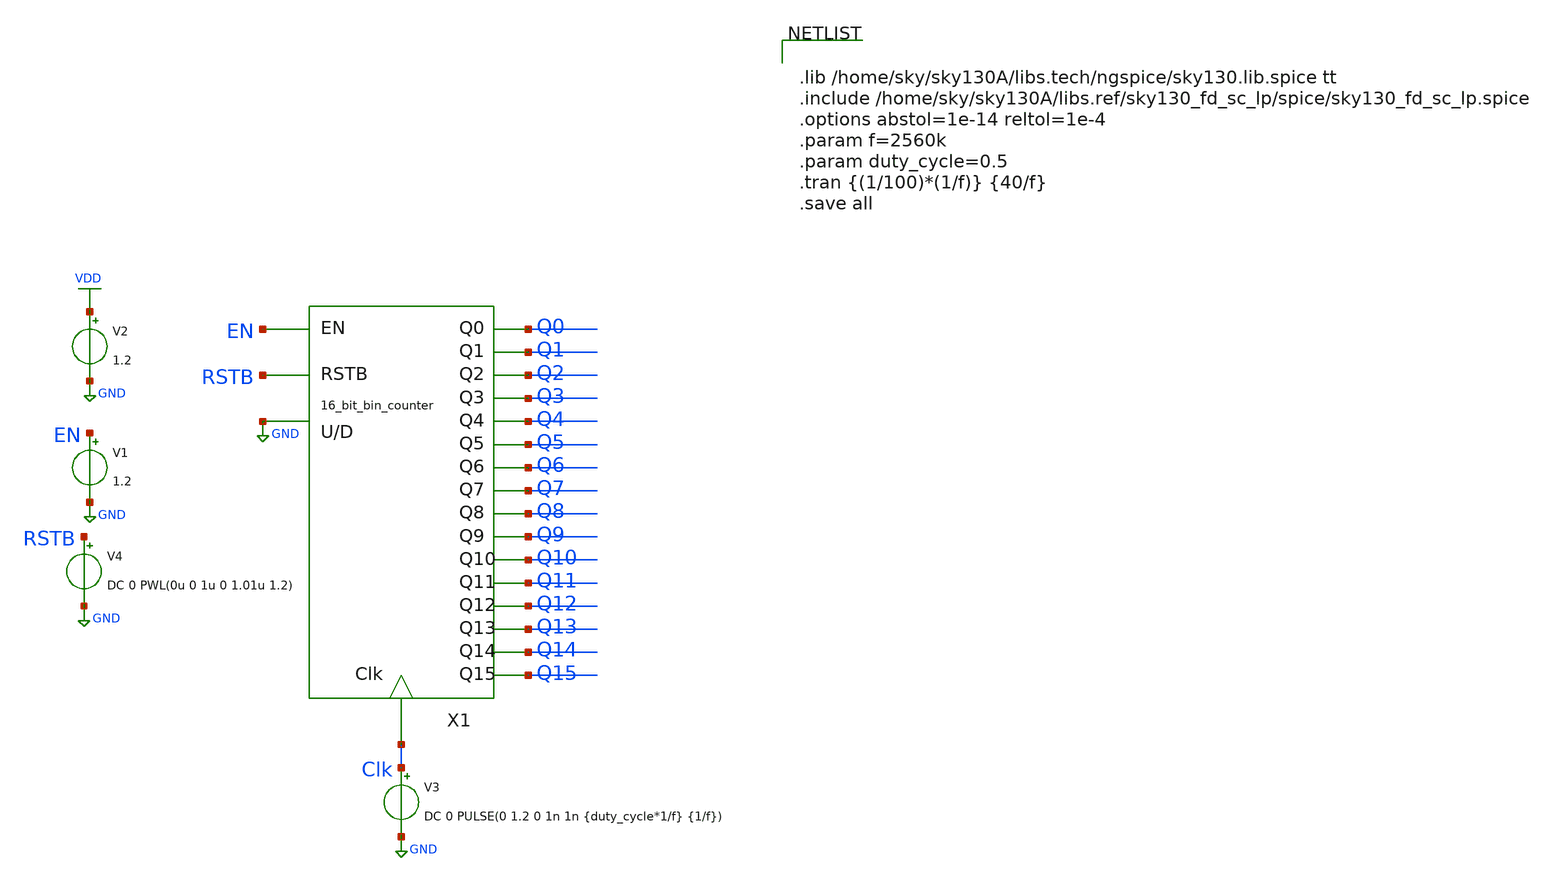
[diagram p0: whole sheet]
** sch_path: xschem/binary counter/bin_counter_tb.sch
**.subckt bin_counter_tb
V3 Clk GND DC 0 PULSE(0 1.2 0 1n 1n {duty_cycle*1/f} {1/f})
V1 EN GND 1.2
V2 VDD GND 1.2
X1 EN Q1 Q6 Clk Q0 Q2 Q3 Q4 Q5 Q7 Q8 Q9 Q10 Q11 Q12 Q13 Q14 Q15 RSTB GND bin_counter
V4 RSTB GND DC 0 PWL(0u 0 1u 0 1.01u 1.2)
**** begin user architecture code


.lib /home/sky/sky130A/libs.tech/ngspice/sky130.lib.spice tt
.include /home/sky/sky130A/libs.ref/sky130_fd_sc_lp/spice/sky130_fd_sc_lp.spice
.options abstol=1e-14 reltol=1e-4
.param f=2560k
.param duty_cycle=0.5
.tran {(1/100)*(1/f)} {40/f}
.save all


**** end user architecture code
**.ends

* expanding   symbol:  binary counter/bin_counter.sym # of pins=20
** sym_path: xschem/binary counter/bin_counter.sym
** sch_path: xschem/binary counter/bin_counter.sch
.subckt bin_counter EN Q1 Q6 Clk Q0 Q2 Q3 Q4 Q5 Q7 Q8 Q9 Q10 Q11 Q12 Q13 Q14 Q15 RSTB U/D
*.ipin Clk
*.ipin EN
*.opin Q0
*.ipin RSTB
*.ipin U/D
*.opin Q1
*.opin Q2
*.opin Q3
*.opin Q4
*.opin Q5
*.opin Q6
*.opin Q7
*.opin Q8
*.opin Q9
*.opin Q10
*.opin Q11
*.opin Q12
*.opin Q13
*.opin Q14
*.opin Q15
x16 U/D Q0 GND GND VDD VDD net1 sky130_fd_sc_lp__and2_1
X17 EN Q0 Clk RSTB net4 asyn_rst_t_ff
x17 net1 net2 GND GND VDD VDD net8 sky130_fd_sc_lp__or2_0
x18 U/D GND GND VDD VDD net3 sky130_fd_sc_lp__inv_1
x19 net4 net3 GND GND VDD VDD net2 sky130_fd_sc_lp__and2_1
x20 net1 Q1 GND GND VDD VDD net5 sky130_fd_sc_lp__and2_1
X18 T1 Q1 Clk RSTB net7 asyn_rst_t_ff
x21 net5 net6 GND GND VDD VDD net48 sky130_fd_sc_lp__or2_0
x23 net7 net2 GND GND VDD VDD net6 sky130_fd_sc_lp__and2_1
x28 net5 Q2 GND GND VDD VDD net9 sky130_fd_sc_lp__and2_1
X20 net62 Q2 Clk RSTB net11 asyn_rst_t_ff
x29 net9 net10 GND GND VDD VDD net50 sky130_fd_sc_lp__or2_0
x31 net11 net6 GND GND VDD VDD net10 sky130_fd_sc_lp__and2_1
x32 net9 Q3 GND GND VDD VDD net12 sky130_fd_sc_lp__and2_1
X21 net63 Q3 Clk RSTB net14 asyn_rst_t_ff
x33 net12 net13 GND GND VDD VDD net51 sky130_fd_sc_lp__or2_0
x35 net14 net10 GND GND VDD VDD net13 sky130_fd_sc_lp__and2_1
x36 net12 Q4 GND GND VDD VDD net15 sky130_fd_sc_lp__and2_1
X22 net64 Q4 Clk RSTB net17 asyn_rst_t_ff
x37 net15 net16 GND GND VDD VDD net49 sky130_fd_sc_lp__or2_0
x39 net17 net13 GND GND VDD VDD net16 sky130_fd_sc_lp__and2_1
x40 net15 Q5 GND GND VDD VDD net18 sky130_fd_sc_lp__and2_1
X23 net65 Q5 Clk RSTB net20 asyn_rst_t_ff
x41 net18 net19 GND GND VDD VDD net52 sky130_fd_sc_lp__or2_0
x43 net20 net16 GND GND VDD VDD net19 sky130_fd_sc_lp__and2_1
x44 net18 Q6 GND GND VDD VDD net21 sky130_fd_sc_lp__and2_1
X24 net66 Q6 Clk RSTB net23 asyn_rst_t_ff
x45 net21 net22 GND GND VDD VDD net53 sky130_fd_sc_lp__or2_0
x47 net23 net19 GND GND VDD VDD net22 sky130_fd_sc_lp__and2_1
x48 net21 Q7 GND GND VDD VDD net24 sky130_fd_sc_lp__and2_1
X25 net67 Q7 Clk RSTB net26 asyn_rst_t_ff
x49 net24 net25 GND GND VDD VDD net54 sky130_fd_sc_lp__or2_0
x51 net26 net22 GND GND VDD VDD net25 sky130_fd_sc_lp__and2_1
x1 net24 Q8 GND GND VDD VDD net27 sky130_fd_sc_lp__and2_1
X1 net68 Q8 Clk RSTB net29 asyn_rst_t_ff
x2 net27 net28 GND GND VDD VDD net55 sky130_fd_sc_lp__or2_0
x4 net29 net25 GND GND VDD VDD net28 sky130_fd_sc_lp__and2_1
x5 net27 Q9 GND GND VDD VDD net30 sky130_fd_sc_lp__and2_1
X2 net69 Q9 Clk RSTB net32 asyn_rst_t_ff
x6 net30 net31 GND GND VDD VDD net56 sky130_fd_sc_lp__or2_0
x8 net32 net28 GND GND VDD VDD net31 sky130_fd_sc_lp__and2_1
x9 net30 Q10 GND GND VDD VDD net33 sky130_fd_sc_lp__and2_1
X3 net70 Q10 Clk RSTB net35 asyn_rst_t_ff
x10 net33 net34 GND GND VDD VDD net57 sky130_fd_sc_lp__or2_0
x12 net35 net31 GND GND VDD VDD net34 sky130_fd_sc_lp__and2_1
x13 net33 Q11 GND GND VDD VDD net36 sky130_fd_sc_lp__and2_1
X4 net71 Q11 Clk RSTB net38 asyn_rst_t_ff
x14 net36 net37 GND GND VDD VDD net58 sky130_fd_sc_lp__or2_0
x52 net38 net34 GND GND VDD VDD net37 sky130_fd_sc_lp__and2_1
x53 net36 Q12 GND GND VDD VDD net39 sky130_fd_sc_lp__and2_1
X5 net72 Q12 Clk RSTB net41 asyn_rst_t_ff
x54 net39 net40 GND GND VDD VDD net59 sky130_fd_sc_lp__or2_0
x56 net41 net37 GND GND VDD VDD net40 sky130_fd_sc_lp__and2_1
x57 net39 Q13 GND GND VDD VDD net42 sky130_fd_sc_lp__and2_1
X6 net73 Q13 Clk RSTB net44 asyn_rst_t_ff
x58 net42 net43 GND GND VDD VDD net60 sky130_fd_sc_lp__or2_0
x60 net44 net40 GND GND VDD VDD net43 sky130_fd_sc_lp__and2_1
x61 net42 Q14 GND GND VDD VDD net45 sky130_fd_sc_lp__and2_1
X7 net74 Q14 Clk RSTB net47 asyn_rst_t_ff
x62 net45 net46 GND GND VDD VDD net61 sky130_fd_sc_lp__or2_0
x64 net47 net43 GND GND VDD VDD net46 sky130_fd_sc_lp__and2_1
X8 net75 RSTB Q15 Q15_N Clk asyn_st_tff
x3 net8 EN GND GND VDD VDD T1 sky130_fd_sc_lp__and2_1
x7 net48 EN GND GND VDD VDD net62 sky130_fd_sc_lp__and2_1
x11 net49 EN GND GND VDD VDD net65 sky130_fd_sc_lp__and2_1
x15 net50 EN GND GND VDD VDD net63 sky130_fd_sc_lp__and2_1
x22 net51 EN GND GND VDD VDD net64 sky130_fd_sc_lp__and2_1
x24 net52 EN GND GND VDD VDD net66 sky130_fd_sc_lp__and2_1
x25 net53 EN GND GND VDD VDD net67 sky130_fd_sc_lp__and2_1
x26 net54 EN GND GND VDD VDD net68 sky130_fd_sc_lp__and2_1
x27 net55 EN GND GND VDD VDD net69 sky130_fd_sc_lp__and2_1
x30 net56 EN GND GND VDD VDD net70 sky130_fd_sc_lp__and2_1
x34 net57 EN GND GND VDD VDD net71 sky130_fd_sc_lp__and2_1
x38 net58 EN GND GND VDD VDD net72 sky130_fd_sc_lp__and2_1
x42 net59 EN GND GND VDD VDD net73 sky130_fd_sc_lp__and2_1
x46 net60 EN GND GND VDD VDD net74 sky130_fd_sc_lp__and2_1
x50 net61 EN GND GND VDD VDD net75 sky130_fd_sc_lp__and2_1
.ends


* expanding   symbol:  T_flip_flop/asyn_rst_t_ff.sym # of pins=5
** sym_path: xschem/T_flip_flop/asyn_rst_t_ff.sym
** sch_path: xschem/T_flip_flop/asyn_rst_t_ff.sch
.subckt asyn_rst_t_ff T Q CLK RSTB Q_N
*.ipin T
*.ipin CLK
*.opin Q
*.ipin RSTB
*.opin Q_N
x3 T Q GND GND VDD VDD net1 sky130_fd_sc_lp__xor2_1
x2 Q GND GND VDD VDD Q_N sky130_fd_sc_lp__inv_1
x4 CLK net1 RSTB GND GND VDD VDD Q sky130_fd_sc_lp__dfrtp_1
.ends


* expanding   symbol:  T_flip_flop/asyn_st_tff.sym # of pins=5
** sym_path: xschem/T_flip_flop/asyn_st_tff.sym
** sch_path: xschem/T_flip_flop/asyn_st_tff.sch
.subckt asyn_st_tff T STB Q Q_N CLK
*.ipin T
*.ipin CLK
*.opin Q
*.ipin STB
*.opin Q_N
x3 T Q GND GND VDD VDD net1 sky130_fd_sc_lp__xor2_1
x1 CLK net1 STB GND GND VDD VDD Q Q_N sky130_fd_sc_lp__dfsbp_1
.ends

.GLOBAL GND
.GLOBAL VDD
.end
